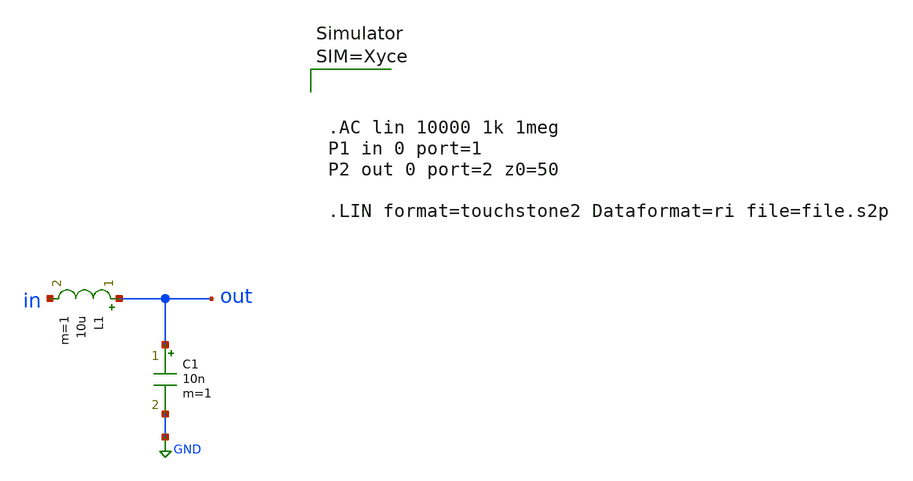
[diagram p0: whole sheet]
** sch_path: ihp-sg13g2/libs.tech/xschem/sg13g2_tests_xyce/cap_test_sparam.sch
* Copyright 2023 IHP PDK Authors
**.subckt cap_test_sparam
C1 out GND 10n m=1
L1 out in 10u m=1
**** begin user architecture code



**** end user architecture code
**.ends
.GLOBAL GND
.end
